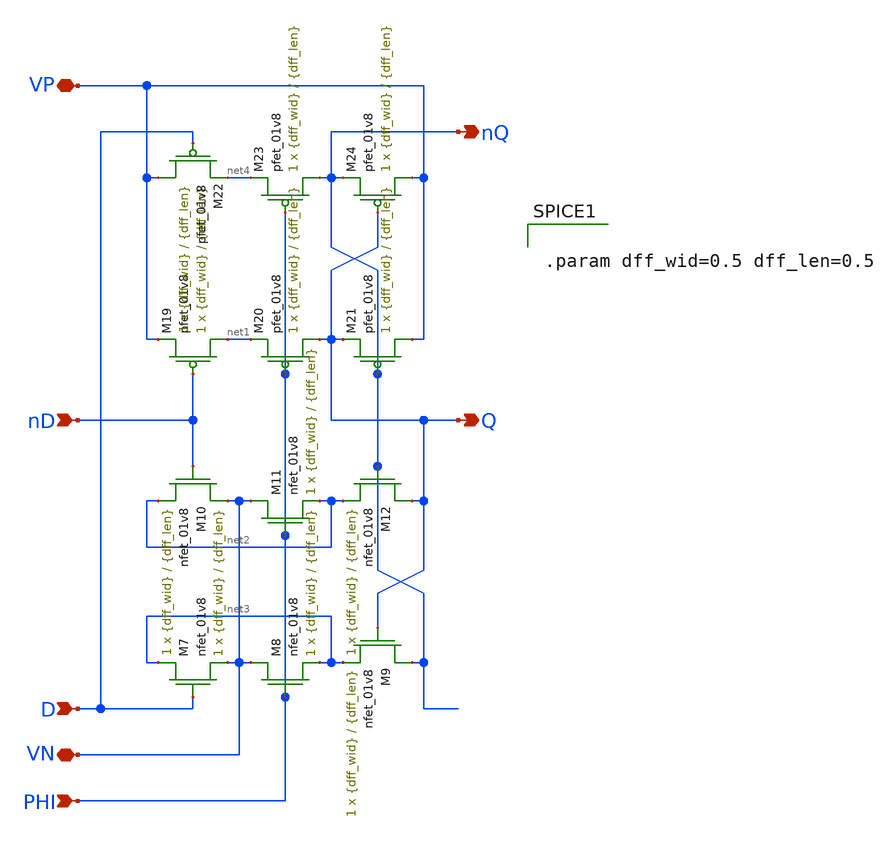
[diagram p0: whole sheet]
** sch_path: LDS/LDS_csrl_latch.sch
**.subckt LDS_csrl_latch nD D Q nQ PHI VP VN
*.ipin nD
*.ipin D
*.opin Q
*.opin nQ
*.ipin PHI
*.iopin VP
*.iopin VN
XM7 net3 D VN VN sky130_fd_pr__nfet_01v8 L={dff_len} W={dff_wid} nf=1 ad='int((nf+1)/2) * W/nf * 0.29'
+ as='int((nf+2)/2) * W/nf * 0.29' pd='2*int((nf+1)/2) * (W/nf + 0.29)' ps='2*int((nf+2)/2) * (W/nf + 0.29)'
+ nrd='0.29 / W' nrs='0.29 / W' sa=0 sb=0 sd=0 mult=1 m=1
XM8 VN PHI net3 VN sky130_fd_pr__nfet_01v8 L={dff_len} W={dff_wid} nf=1 ad='int((nf+1)/2) * W/nf * 0.29'
+ as='int((nf+2)/2) * W/nf * 0.29' pd='2*int((nf+1)/2) * (W/nf + 0.29)' ps='2*int((nf+2)/2) * (W/nf + 0.29)'
+ nrd='0.29 / W' nrs='0.29 / W' sa=0 sb=0 sd=0 mult=1 m=1
XM9 nQ Q net3 VN sky130_fd_pr__nfet_01v8 L={dff_len} W={dff_wid} nf=1 ad='int((nf+1)/2) * W/nf * 0.29'
+ as='int((nf+2)/2) * W/nf * 0.29' pd='2*int((nf+1)/2) * (W/nf + 0.29)' ps='2*int((nf+2)/2) * (W/nf + 0.29)'
+ nrd='0.29 / W' nrs='0.29 / W' sa=0 sb=0 sd=0 mult=1 m=1
XM10 VN nD net2 VN sky130_fd_pr__nfet_01v8 L={dff_len} W={dff_wid} nf=1 ad='int((nf+1)/2) * W/nf * 0.29'
+ as='int((nf+2)/2) * W/nf * 0.29' pd='2*int((nf+1)/2) * (W/nf + 0.29)' ps='2*int((nf+2)/2) * (W/nf + 0.29)'
+ nrd='0.29 / W' nrs='0.29 / W' sa=0 sb=0 sd=0 mult=1 m=1
XM11 VN PHI net2 VN sky130_fd_pr__nfet_01v8 L={dff_len} W={dff_wid} nf=1 ad='int((nf+1)/2) * W/nf * 0.29'
+ as='int((nf+2)/2) * W/nf * 0.29' pd='2*int((nf+1)/2) * (W/nf + 0.29)' ps='2*int((nf+2)/2) * (W/nf + 0.29)'
+ nrd='0.29 / W' nrs='0.29 / W' sa=0 sb=0 sd=0 mult=1 m=1
XM12 Q nQ net2 VN sky130_fd_pr__nfet_01v8 L={dff_len} W={dff_wid} nf=1 ad='int((nf+1)/2) * W/nf * 0.29'
+ as='int((nf+2)/2) * W/nf * 0.29' pd='2*int((nf+1)/2) * (W/nf + 0.29)' ps='2*int((nf+2)/2) * (W/nf + 0.29)'
+ nrd='0.29 / W' nrs='0.29 / W' sa=0 sb=0 sd=0 mult=1 m=1
XM19 net1 nD VP VP sky130_fd_pr__pfet_01v8 L={dff_len} W={dff_wid} nf=1 ad='int((nf+1)/2) * W/nf * 0.29'
+ as='int((nf+2)/2) * W/nf * 0.29' pd='2*int((nf+1)/2) * (W/nf + 0.29)' ps='2*int((nf+2)/2) * (W/nf + 0.29)'
+ nrd='0.29 / W' nrs='0.29 / W' sa=0 sb=0 sd=0 mult=1 m=1
XM20 Q PHI net1 VP sky130_fd_pr__pfet_01v8 L={dff_len} W={dff_wid} nf=1 ad='int((nf+1)/2) * W/nf * 0.29'
+ as='int((nf+2)/2) * W/nf * 0.29' pd='2*int((nf+1)/2) * (W/nf + 0.29)' ps='2*int((nf+2)/2) * (W/nf + 0.29)'
+ nrd='0.29 / W' nrs='0.29 / W' sa=0 sb=0 sd=0 mult=1 m=1
XM21 VP nQ Q VP sky130_fd_pr__pfet_01v8 L={dff_len} W={dff_wid} nf=1 ad='int((nf+1)/2) * W/nf * 0.29'
+ as='int((nf+2)/2) * W/nf * 0.29' pd='2*int((nf+1)/2) * (W/nf + 0.29)' ps='2*int((nf+2)/2) * (W/nf + 0.29)'
+ nrd='0.29 / W' nrs='0.29 / W' sa=0 sb=0 sd=0 mult=1 m=1
XM22 VP D net4 VP sky130_fd_pr__pfet_01v8 L={dff_len} W={dff_wid} nf=1 ad='int((nf+1)/2) * W/nf * 0.29'
+ as='int((nf+2)/2) * W/nf * 0.29' pd='2*int((nf+1)/2) * (W/nf + 0.29)' ps='2*int((nf+2)/2) * (W/nf + 0.29)'
+ nrd='0.29 / W' nrs='0.29 / W' sa=0 sb=0 sd=0 mult=1 m=1
XM23 nQ PHI net4 VP sky130_fd_pr__pfet_01v8 L={dff_len} W={dff_wid} nf=1 ad='int((nf+1)/2) * W/nf * 0.29'
+ as='int((nf+2)/2) * W/nf * 0.29' pd='2*int((nf+1)/2) * (W/nf + 0.29)' ps='2*int((nf+2)/2) * (W/nf + 0.29)'
+ nrd='0.29 / W' nrs='0.29 / W' sa=0 sb=0 sd=0 mult=1 m=1
XM24 VP Q nQ VP sky130_fd_pr__pfet_01v8 L={dff_len} W={dff_wid} nf=1 ad='int((nf+1)/2) * W/nf * 0.29'
+ as='int((nf+2)/2) * W/nf * 0.29' pd='2*int((nf+1)/2) * (W/nf + 0.29)' ps='2*int((nf+2)/2) * (W/nf + 0.29)'
+ nrd='0.29 / W' nrs='0.29 / W' sa=0 sb=0 sd=0 mult=1 m=1
**** begin user architecture code


.param dff_wid=0.5 dff_len=0.5


**** end user architecture code
**.ends
.end
